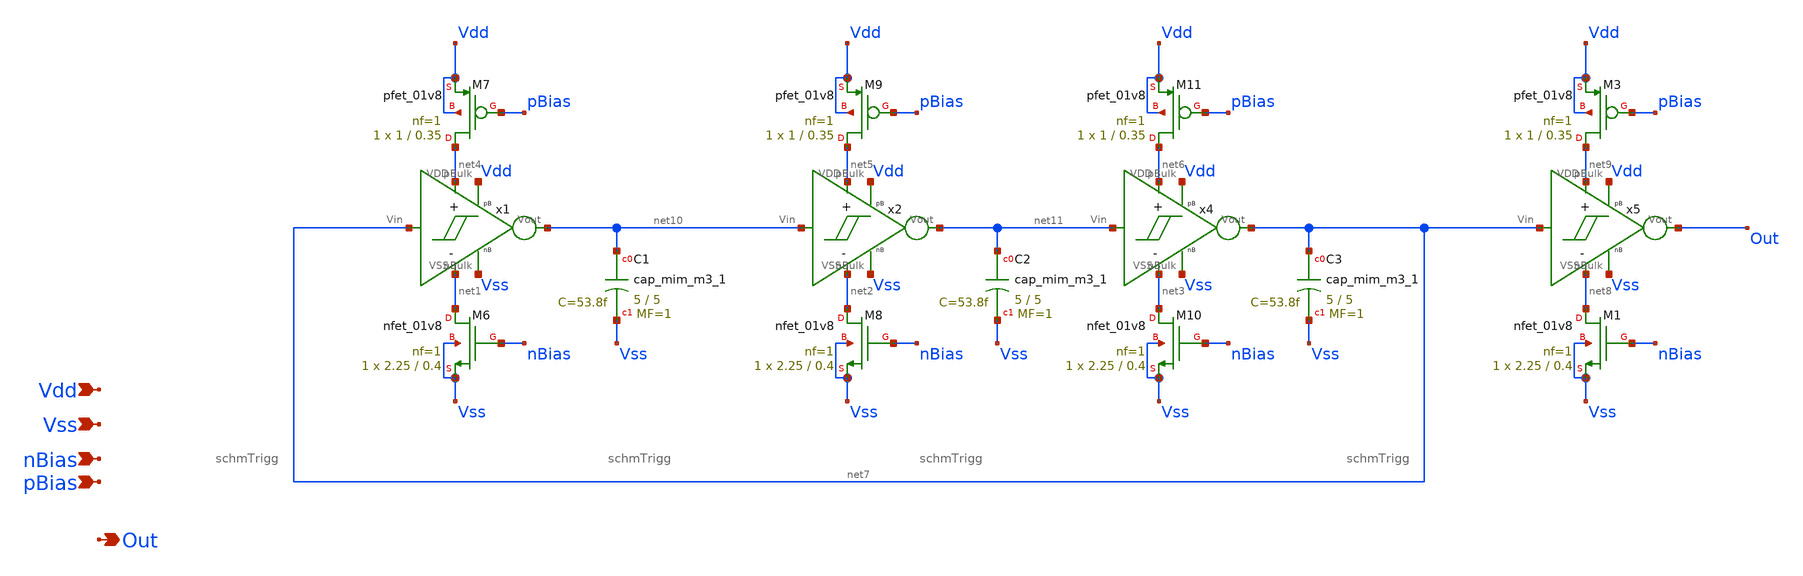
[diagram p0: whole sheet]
** sch_path: tt10-hdl/tt_um_test_commit/xschem/T3/oscillators/A_tt10_Ring_currentStarved/osc.sch
**.subckt osc Vdd Vss Out nBias pBias
*.ipin Vdd
*.ipin Vss
*.opin Out
*.ipin nBias
*.ipin pBias
XM6 net1 nBias Vss Vss sky130_fd_pr__nfet_01v8 L=0.4 W=2.25 nf=1 ad='int((1 + 1)/2) * 2.25 / 1 * 0.29'
+ as='int((1 + 2)/2) * 2.25 / 1 * 0.29' pd='2*int((1 + 1)/2) * (2.25 / 1 + 0.29)' ps='2*int((1 + 2)/2) * (2.25 / 1 + 0.29)'
+ nrd='0.29 / 2.25 ' nrs='0.29 / 2.25 ' sa=0 sb=0 sd=0 mult=1 m=1
XM7 net4 pBias Vdd Vdd sky130_fd_pr__pfet_01v8 L=0.35 W=1 nf=1 ad='int((nf+1)/2) * W/nf * 0.29' as='int((nf+2)/2) * W/nf * 0.29'
+ pd='2*int((nf+1)/2) * (W/nf + 0.29)' ps='2*int((nf+2)/2) * (W/nf + 0.29)' nrd='0.29 / W' nrs='0.29 / W'
+ sa=0 sb=0 sd=0 mult=1 m=1
XM8 net2 nBias Vss Vss sky130_fd_pr__nfet_01v8 L=0.4 W=2.25 nf=1 ad='int((1 + 1)/2) * 2.25 / 1 * 0.29'
+ as='int((1 + 2)/2) * 2.25 / 1 * 0.29' pd='2*int((1 + 1)/2) * (2.25 / 1 + 0.29)' ps='2*int((1 + 2)/2) * (2.25 / 1 + 0.29)'
+ nrd='0.29 / 2.25 ' nrs='0.29 / 2.25 ' sa=0 sb=0 sd=0 mult=1 m=1
XM9 net5 pBias Vdd Vdd sky130_fd_pr__pfet_01v8 L=0.35 W=1 nf=1 ad='int((nf+1)/2) * W/nf * 0.29' as='int((nf+2)/2) * W/nf * 0.29'
+ pd='2*int((nf+1)/2) * (W/nf + 0.29)' ps='2*int((nf+2)/2) * (W/nf + 0.29)' nrd='0.29 / W' nrs='0.29 / W'
+ sa=0 sb=0 sd=0 mult=1 m=1
XM10 net3 nBias Vss Vss sky130_fd_pr__nfet_01v8 L=0.4 W=2.25 nf=1 ad='int((1 + 1)/2) * 2.25 / 1 * 0.29'
+ as='int((1 + 2)/2) * 2.25 / 1 * 0.29' pd='2*int((1 + 1)/2) * (2.25 / 1 + 0.29)' ps='2*int((1 + 2)/2) * (2.25 / 1 + 0.29)'
+ nrd='0.29 / 2.25 ' nrs='0.29 / 2.25 ' sa=0 sb=0 sd=0 mult=1 m=1
XM11 net6 pBias Vdd Vdd sky130_fd_pr__pfet_01v8 L=0.35 W=1 nf=1 ad='int((nf+1)/2) * W/nf * 0.29' as='int((nf+2)/2) * W/nf * 0.29'
+ pd='2*int((nf+1)/2) * (W/nf + 0.29)' ps='2*int((nf+2)/2) * (W/nf + 0.29)' nrd='0.29 / W' nrs='0.29 / W'
+ sa=0 sb=0 sd=0 mult=1 m=1
x2 net10 net2 net5 net11 Vdd Vss schmTrigg
x1 net7 net1 net4 net10 Vdd Vss schmTrigg
x4 net11 net3 net6 net7 Vdd Vss schmTrigg
XM1 net8 nBias Vss Vss sky130_fd_pr__nfet_01v8 L=0.4 W=2.25 nf=1 ad='int((1 + 1)/2) * 2.25 / 1 * 0.29'
+ as='int((1 + 2)/2) * 2.25 / 1 * 0.29' pd='2*int((1 + 1)/2) * (2.25 / 1 + 0.29)' ps='2*int((1 + 2)/2) * (2.25 / 1 + 0.29)'
+ nrd='0.29 / 2.25 ' nrs='0.29 / 2.25 ' sa=0 sb=0 sd=0 mult=1 m=1
XM3 net9 pBias Vdd Vdd sky130_fd_pr__pfet_01v8 L=0.35 W=1 nf=1 ad='int((nf+1)/2) * W/nf * 0.29' as='int((nf+2)/2) * W/nf * 0.29'
+ pd='2*int((nf+1)/2) * (W/nf + 0.29)' ps='2*int((nf+2)/2) * (W/nf + 0.29)' nrd='0.29 / W' nrs='0.29 / W'
+ sa=0 sb=0 sd=0 mult=1 m=1
x5 net7 net8 net9 Out Vdd Vss schmTrigg
XC1 net10 Vss sky130_fd_pr__cap_mim_m3_1 W=5 L=5 MF=1 m=1
XC2 net11 Vss sky130_fd_pr__cap_mim_m3_1 W=5 L=5 MF=1 m=1
XC3 net7 Vss sky130_fd_pr__cap_mim_m3_1 W=5 L=5 MF=1 m=1
**.ends

* expanding   symbol:  T1/schmTrigg/schmTrigg.sym # of pins=6
** sym_path: tt10-hdl/tt_um_test_commit/xschem/T1/schmTrigg/schmTrigg.sym
** sch_path: tt10-hdl/tt_um_test_commit/xschem/T1/schmTrigg/schmTrigg.sch
.subckt schmTrigg Vin VSS VDD Vout pBulk nBulk
*.ipin Vin
*.ipin VDD
*.ipin VSS
*.opin Vout
*.ipin nBulk
*.ipin pBulk
XM1 VDD Vout Vn nBulk sky130_fd_pr__nfet_01v8 L=0.15 W=1 nf=1 ad='int((1 + 1)/2) * 1 / 1 * 0.29' as='int((1 + 2)/2) * 1 / 1 * 0.29'
+ pd='2*int((1 + 1)/2) * (1 / 1 + 0.29)' ps='2*int((1 + 2)/2) * (1 / 1 + 0.29)' nrd='0.29 / 1 ' nrs='0.29 / 1 '
+ sa=0 sb=0 sd=0 mult=1 m=1
XM2 Vn Vin VSS nBulk sky130_fd_pr__nfet_01v8 L=0.15 W=1 nf=1 ad='int((1 + 1)/2) * 1 / 1 * 0.29' as='int((1 + 2)/2) * 1 / 1 * 0.29'
+ pd='2*int((1 + 1)/2) * (1 / 1 + 0.29)' ps='2*int((1 + 2)/2) * (1 / 1 + 0.29)' nrd='0.29 / 1 ' nrs='0.29 / 1 '
+ sa=0 sb=0 sd=0 mult=1 m=1
XM3 Vout Vin Vn nBulk sky130_fd_pr__nfet_01v8 L=0.15 W=1 nf=1 ad='int((1 + 1)/2) * 1 / 1 * 0.29' as='int((1 + 2)/2) * 1 / 1 * 0.29'
+ pd='2*int((1 + 1)/2) * (1 / 1 + 0.29)' ps='2*int((1 + 2)/2) * (1 / 1 + 0.29)' nrd='0.29 / 1 ' nrs='0.29 / 1 '
+ sa=0 sb=0 sd=0 mult=1 m=1
XM4 VSS Vout Vp pBulk sky130_fd_pr__pfet_01v8 L=0.15 W=1 nf=1 ad='int((nf+1)/2) * W/nf * 0.29' as='int((nf+2)/2) * W/nf * 0.29'
+ pd='2*int((nf+1)/2) * (W/nf + 0.29)' ps='2*int((nf+2)/2) * (W/nf + 0.29)' nrd='0.29 / W' nrs='0.29 / W'
+ sa=0 sb=0 sd=0 mult=1 m=1
XM5 Vout Vin Vp pBulk sky130_fd_pr__pfet_01v8 L=0.15 W=1 nf=1 ad='int((nf+1)/2) * W/nf * 0.29' as='int((nf+2)/2) * W/nf * 0.29'
+ pd='2*int((nf+1)/2) * (W/nf + 0.29)' ps='2*int((nf+2)/2) * (W/nf + 0.29)' nrd='0.29 / W' nrs='0.29 / W'
+ sa=0 sb=0 sd=0 mult=1 m=1
XM6 Vp Vin VDD pBulk sky130_fd_pr__pfet_01v8 L=0.15 W=1 nf=1 ad='int((nf+1)/2) * W/nf * 0.29' as='int((nf+2)/2) * W/nf * 0.29'
+ pd='2*int((nf+1)/2) * (W/nf + 0.29)' ps='2*int((nf+2)/2) * (W/nf + 0.29)' nrd='0.29 / W' nrs='0.29 / W'
+ sa=0 sb=0 sd=0 mult=1 m=1
.ends

.end
